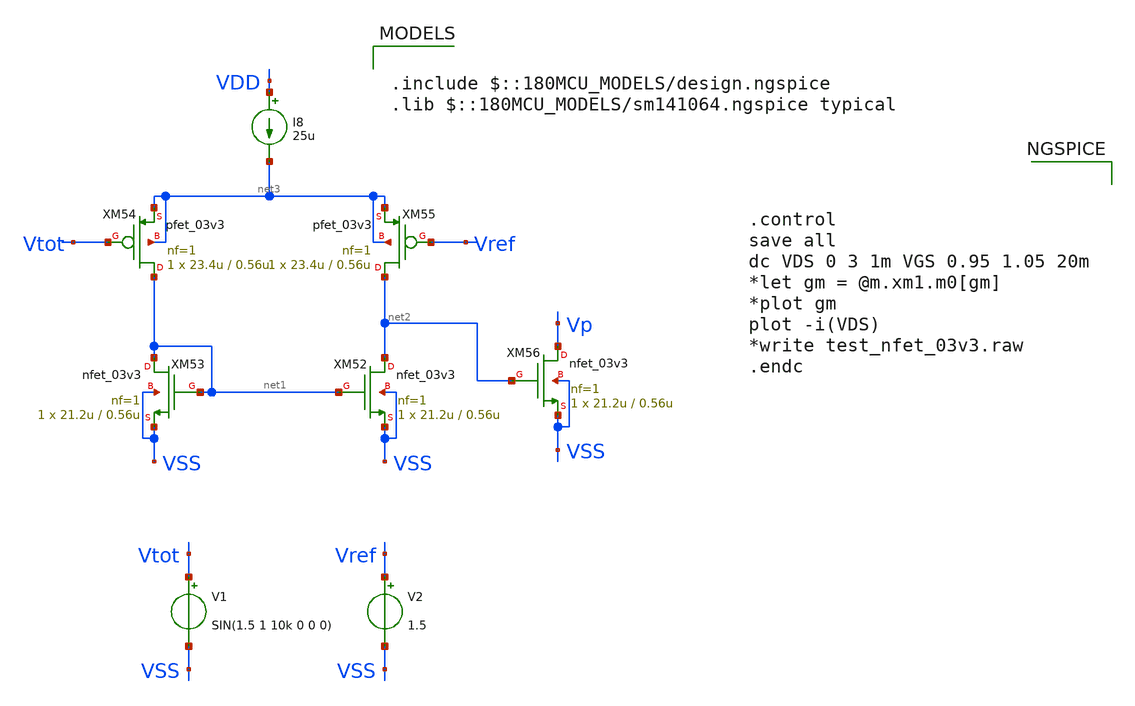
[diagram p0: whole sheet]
** sch_path: SCOP_INPUT_AND_MUX_PAKISTAN_03/Xschem/Others/error_OTA.sch
**.subckt error_OTA
XM52 net2 net1 VSS VSS nfet_03v3 L=0.56u W=21.2u nf=1 ad='int((nf+1)/2) * W/nf * 0.18u' as='int((nf+2)/2) * W/nf * 0.18u'
+ pd='2*int((nf+1)/2) * (W/nf + 0.18u)' ps='2*int((nf+2)/2) * (W/nf + 0.18u)' nrd='0.18u / W' nrs='0.18u / W'
+ sa=0 sb=0 sd=0 m=1
XM53 net1 net1 VSS VSS nfet_03v3 L=0.56u W=21.2u nf=1 ad='int((nf+1)/2) * W/nf * 0.18u' as='int((nf+2)/2) * W/nf * 0.18u'
+ pd='2*int((nf+1)/2) * (W/nf + 0.18u)' ps='2*int((nf+2)/2) * (W/nf + 0.18u)' nrd='0.18u / W' nrs='0.18u / W'
+ sa=0 sb=0 sd=0 m=1
XM54 net1 Vtot net3 net3 pfet_03v3 L=0.56u W=23.4u nf=1 ad='int((nf+1)/2) * W/nf * 0.18u' as='int((nf+2)/2) * W/nf * 0.18u'
+ pd='2*int((nf+1)/2) * (W/nf + 0.18u)' ps='2*int((nf+2)/2) * (W/nf + 0.18u)' nrd='0.18u / W' nrs='0.18u / W'
+ sa=0 sb=0 sd=0 m=1
XM55 net2 Vref net3 net3 pfet_03v3 L=0.56u W=23.4u nf=1 ad='int((nf+1)/2) * W/nf * 0.18u' as='int((nf+2)/2) * W/nf * 0.18u'
+ pd='2*int((nf+1)/2) * (W/nf + 0.18u)' ps='2*int((nf+2)/2) * (W/nf + 0.18u)' nrd='0.18u / W' nrs='0.18u / W'
+ sa=0 sb=0 sd=0 m=1
I8 VDD net3 25u
XM56 Vp net2 VSS VSS nfet_03v3 L=0.56u W=21.2u nf=1 ad='int((nf+1)/2) * W/nf * 0.18u' as='int((nf+2)/2) * W/nf * 0.18u'
+ pd='2*int((nf+1)/2) * (W/nf + 0.18u)' ps='2*int((nf+2)/2) * (W/nf + 0.18u)' nrd='0.18u / W' nrs='0.18u / W'
+ sa=0 sb=0 sd=0 m=1
V1 Vtot VSS SIN(1.5 1 10k 0 0 0)
V2 Vref VSS 1.5
**** begin user architecture code



.control
save all
dc VDS 0 3 1m VGS 0.95 1.05 20m
*let gm = @m.xm1.m0[gm]
*plot gm
plot -i(VDS)
*write test_nfet_03v3.raw
.endc



.include $::180MCU_MODELS/design.ngspice
.lib $::180MCU_MODELS/sm141064.ngspice typical

**** end user architecture code
**.ends
.end
